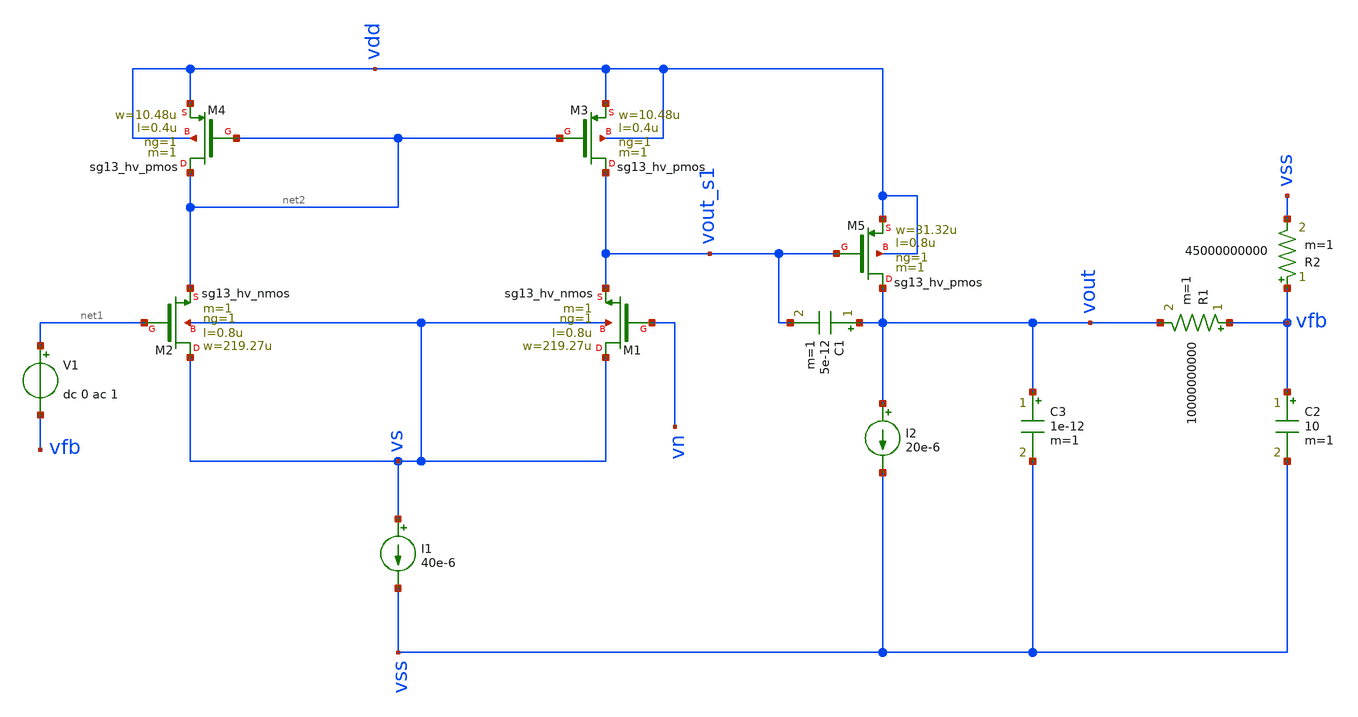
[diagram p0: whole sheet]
** sch_path: test/Tesis_notebooks/xschem/ota_2stage_tb.sch
**.subckt ota_2stage_tb
I1 vs vss 40e-6
I2 vout vss 20e-6
XM1 vs vn vout_s1 vs sg13_hv_nmos w=219.27u l=0.8u ng=1 m=1 mm_ok=1
XM2 vs net1 net2 vs sg13_hv_nmos w=219.27u l=0.8u ng=1 m=1 mm_ok=1
XM3 vout_s1 net2 vdd vdd sg13_hv_pmos w=10.48u l=0.4u ng=1 m=1 mm_ok=1
XM4 net2 net2 vdd vdd sg13_hv_pmos w=10.48u l=0.4u ng=1 m=1 mm_ok=1
XM5 vout vout_s1 vdd vdd sg13_hv_pmos w=31.32u l=0.8u ng=1 m=1 mm_ok=1
R1 vfb vout 10000000000 m=1
C2 vfb vss 10 m=1
R2 vfb vss 45000000000 m=1
V1 net1 vfb dc 0 ac 1
C1 vout vout_s1 5e-12 m=1
C3 vout vss 1e-12 m=1
**** begin user architecture code



.lib /opt/pdks/ihp-sg13g2/libs.tech/ngspice/models/cornerMOShv.lib mos_tt

Vref vn 0 1.35
Vdd vdd 0 3.3
Vss vss 0 0

.control
ac dec 10 1 1G
plot vdb(vout)
plot phase(vout)*180/PI
op
print vout vs vout_s1 vfb
.endc



**** end user architecture code
**.ends
.end
